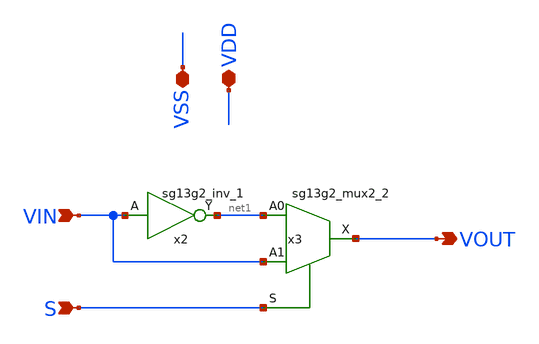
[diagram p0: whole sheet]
** sch_path: example/example_dig.sch
**.subckt example_dig VDD VSS VIN VOUT S
*.iopin VDD
*.iopin VSS
*.ipin VIN
*.opin VOUT
*.ipin S
x2 net1 VIN VDD VSS sg13g2_inv_1
x3 VOUT net1 VIN S VDD VSS sg13g2_mux2_2
**.ends

* expanding   symbol:  sg13g2_stdcells/sg13g2_inv_1.sym # of pins=2
** sym_path: sg13g2_stdcells/sg13g2_inv_1.sym
** sch_path: sg13g2_stdcells/sg13g2_inv_1.sch
.subckt sg13g2_inv_1 Y A VDD VSS
*.opin Y
*.ipin A
*.iopin VDD
*.iopin VSS
XM1 Y A VSS VSS sg13_lv_nmos w=740.00n l=130.00n ng=1 m=1 mm_ok=1
XM2 Y A VDD VDD sg13_lv_pmos w=1.12u l=130.00n ng=1 m=1 mm_ok=1
.ends


* expanding   symbol:  sg13g2_stdcells/sg13g2_mux2_2.sym # of pins=4
** sym_path: sg13g2_stdcells/sg13g2_mux2_2.sym
** sch_path: sg13g2_stdcells/sg13g2_mux2_2.sch
.subckt sg13g2_mux2_2 X A0 A1 S VDD VSS
*.ipin S
*.ipin A0
*.ipin A1
*.opin X
*.iopin VDD
*.iopin VSS
XM1 Sb S VSS VSS sg13_lv_nmos w=550.00n l=130.00n ng=1 m=1 mm_ok=1
XM2 net1 A0 net5 VSS sg13_lv_nmos w=740.00n l=130.00n ng=1 m=1 mm_ok=1
XM3 net5 Sb VSS VSS sg13_lv_nmos w=740.00n l=130.00n ng=1 m=1 mm_ok=1
XM4 net1 A1 net4 VSS sg13_lv_nmos w=740.00n l=130.00n ng=1 m=1 mm_ok=1
XM5 net4 S VSS VSS sg13_lv_nmos w=740.00n l=130.00n ng=1 m=1 mm_ok=1
XM6 X net1 VSS VSS sg13_lv_nmos w=1.48u l=130.00n ng=2 m=1 mm_ok=1
XM7 Sb S VDD VDD sg13_lv_pmos w=840.00n l=130.00n ng=1 m=1 mm_ok=1
XM8 net2 S VDD VDD sg13_lv_pmos w=1.000u l=130.00n ng=1 m=1 mm_ok=1
XM9 net1 A0 net2 VDD sg13_lv_pmos w=1.000u l=130.00n ng=1 m=1 mm_ok=1
XM10 net3 Sb VDD VDD sg13_lv_pmos w=1.000u l=130.00n ng=1 m=1 mm_ok=1
XM11 net1 A1 net3 VDD sg13_lv_pmos w=1.000u l=130.00n ng=1 m=1 mm_ok=1
XM12 X net1 VDD VDD sg13_lv_pmos w=2.24u l=130.00n ng=2 m=1 mm_ok=1
.ends

.end
